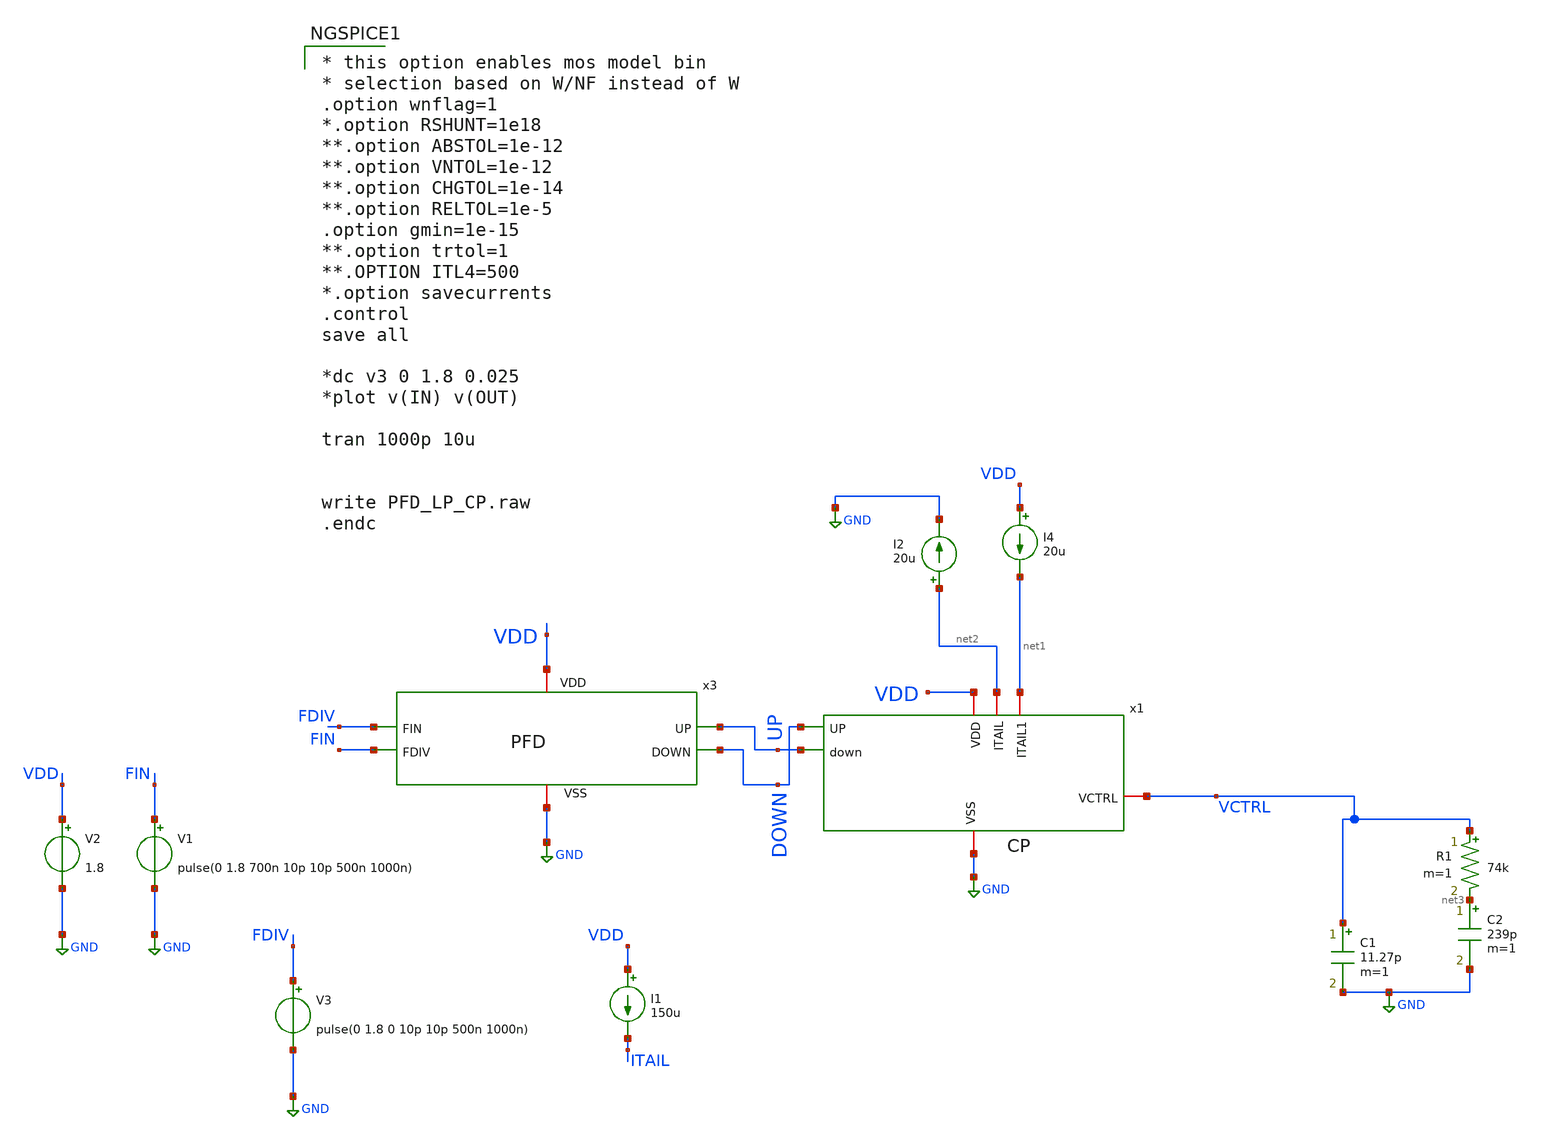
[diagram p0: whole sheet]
** sch_path: Xschem/CP_LP_PFD/PFD_LP_CP.sch
**.subckt PFD_LP_CP
x1 VDD net2 net1 VCTRL DOWN UP GND CP
x3 VDD GND FDIV FIN UP DOWN PFD
C1 VCTRL GND 11.27p m=1
R1 VCTRL net3 74k m=1
C2 net3 GND 239p m=1
V2 VDD GND 1.8
V1 FIN GND pulse(0 1.8 700n 10p 10p 500n 1000n)
V3 FDIV GND pulse(0 1.8 0 10p 10p 500n 1000n)
I1 VDD ITAIL 150u
I4 VDD net1 20u
I2 net2 GND 20u
**** begin user architecture code

** opencircuitdesign pdks install
.lib $::SKYWATER_MODELS/sky130.lib.spice tt



* this option enables mos model bin
* selection based on W/NF instead of W
.option wnflag=1
*.option RSHUNT=1e18
**.option ABSTOL=1e-12
**.option VNTOL=1e-12
**.option CHGTOL=1e-14
**.option RELTOL=1e-5
.option gmin=1e-15
**.option trtol=1
**.OPTION ITL4=500
*.option savecurrents
.control
save all

*dc v3 0 1.8 0.025
*plot v(IN) v(OUT)

tran 1000p 10u


write PFD_LP_CP.raw
.endc


**** end user architecture code
**.ends

* expanding   symbol:  CP.sym # of pins=7
** sym_path: CP.sym
** sch_path: CP.sch
.subckt CP VDD ITAIL ITAIL1 VCTRL UP down VSS
*.ipin UP
*.ipin down
*.iopin VCTRL
*.iopin VDD
*.iopin VSS
*.iopin ITAIL1
*.iopin ITAIL
XM8 net2 UP VDD VDD sky130_fd_pr__pfet_01v8 L=0.5 W=1 nf=1 ad='int((nf+1)/2) * W/nf * 0.29' as='int((nf+2)/2) * W/nf * 0.29'
+ pd='2*int((nf+1)/2) * (W/nf + 0.29)' ps='2*int((nf+2)/2) * (W/nf + 0.29)' nrd='0.29 / W' nrs='0.29 / W'
+ sa=0 sb=0 sd=0 mult=1 m=1
XM1 net1 net2 VDD VDD sky130_fd_pr__pfet_01v8 L=0.5 W=3 nf=1 ad='int((nf+1)/2) * W/nf * 0.29' as='int((nf+2)/2) * W/nf * 0.29'
+ pd='2*int((nf+1)/2) * (W/nf + 0.29)' ps='2*int((nf+2)/2) * (W/nf + 0.29)' nrd='0.29 / W' nrs='0.29 / W'
+ sa=0 sb=0 sd=0 mult=1 m=1
XM10 net2 UP VSS VSS sky130_fd_pr__nfet_01v8 L=0.5 W=0.5 nf=1 ad='int((nf+1)/2) * W/nf * 0.29' as='int((nf+2)/2) * W/nf * 0.29'
+ pd='2*int((nf+1)/2) * (W/nf + 0.29)' ps='2*int((nf+2)/2) * (W/nf + 0.29)' nrd='0.29 / W' nrs='0.29 / W'
+ sa=0 sb=0 sd=0 mult=1 m=1
XM2 VCTRL ITAIL net1 VDD sky130_fd_pr__pfet_01v8 L=0.5 W=2.5 nf=1 ad='int((nf+1)/2) * W/nf * 0.29' as='int((nf+2)/2) * W/nf * 0.29'
+ pd='2*int((nf+1)/2) * (W/nf + 0.29)' ps='2*int((nf+2)/2) * (W/nf + 0.29)' nrd='0.29 / W' nrs='0.29 / W'
+ sa=0 sb=0 sd=0 mult=1 m=1
XM3 ITAIL ITAIL VDD VDD sky130_fd_pr__pfet_01v8 L=0.5 W=2.5 nf=1 ad='int((nf+1)/2) * W/nf * 0.29' as='int((nf+2)/2) * W/nf * 0.29'
+ pd='2*int((nf+1)/2) * (W/nf + 0.29)' ps='2*int((nf+2)/2) * (W/nf + 0.29)' nrd='0.29 / W' nrs='0.29 / W'
+ sa=0 sb=0 sd=0 mult=1 m=1
XM5 ITAIL1 ITAIL1 VSS VSS sky130_fd_pr__nfet_01v8 L=0.5 W=1.5 nf=1 ad='int((nf+1)/2) * W/nf * 0.29' as='int((nf+2)/2) * W/nf * 0.29'
+ pd='2*int((nf+1)/2) * (W/nf + 0.29)' ps='2*int((nf+2)/2) * (W/nf + 0.29)' nrd='0.29 / W' nrs='0.29 / W'
+ sa=0 sb=0 sd=0 mult=1 m=1
XM6 VCTRL ITAIL1 net3 VSS sky130_fd_pr__nfet_01v8 L=0.5 W=1.5 nf=1 ad='int((nf+1)/2) * W/nf * 0.29' as='int((nf+2)/2) * W/nf * 0.29'
+ pd='2*int((nf+1)/2) * (W/nf + 0.29)' ps='2*int((nf+2)/2) * (W/nf + 0.29)' nrd='0.29 / W' nrs='0.29 / W'
+ sa=0 sb=0 sd=0 mult=1 m=1
XM4 net3 down VSS VSS sky130_fd_pr__nfet_01v8 L=0.5 W=1.5 nf=1 ad='int((nf+1)/2) * W/nf * 0.29' as='int((nf+2)/2) * W/nf * 0.29'
+ pd='2*int((nf+1)/2) * (W/nf + 0.29)' ps='2*int((nf+2)/2) * (W/nf + 0.29)' nrd='0.29 / W' nrs='0.29 / W'
+ sa=0 sb=0 sd=0 mult=1 m=1
.ends


* expanding   symbol:  PFD.sym # of pins=6
** sym_path: xschem/PFD.sym
** sch_path: xschem/PFD.sch
.subckt PFD VDD VSS FDIV FIN UP DOWN
*.ipin FDIV
*.ipin FIN
*.opin UP
*.opin DOWN
*.iopin VSS
*.iopin VDD
XM2 A FIN VDD VDD sky130_fd_pr__pfet_01v8 L=0.15 W=0.6 nf=1 ad='int((nf+1)/2) * W/nf * 0.29' as='int((nf+2)/2) * W/nf * 0.29'
+ pd='2*int((nf+1)/2) * (W/nf + 0.29)' ps='2*int((nf+2)/2) * (W/nf + 0.29)' nrd='0.29 / W' nrs='0.29 / W'
+ sa=0 sb=0 sd=0 mult=1 m=1
XM3 x1 A VDD VDD sky130_fd_pr__pfet_01v8 L=0.15 W=2.4 nf=1 ad='int((nf+1)/2) * W/nf * 0.29' as='int((nf+2)/2) * W/nf * 0.29'
+ pd='2*int((nf+1)/2) * (W/nf + 0.29)' ps='2*int((nf+2)/2) * (W/nf + 0.29)' nrd='0.29 / W' nrs='0.29 / W'
+ sa=0 sb=0 sd=0 mult=1 m=1
XM4 x1 x1 net1 VDD sky130_fd_pr__pfet_01v8 L=0.15 W=0.9 nf=1 ad='int((nf+1)/2) * W/nf * 0.29' as='int((nf+2)/2) * W/nf * 0.29'
+ pd='2*int((nf+1)/2) * (W/nf + 0.29)' ps='2*int((nf+2)/2) * (W/nf + 0.29)' nrd='0.29 / W' nrs='0.29 / W'
+ sa=0 sb=0 sd=0 mult=1 m=1
XM5 net1 x2 VDD VDD sky130_fd_pr__pfet_01v8 L=0.15 W=0.9 nf=1 ad='int((nf+1)/2) * W/nf * 0.29' as='int((nf+2)/2) * W/nf * 0.29'
+ pd='2*int((nf+1)/2) * (W/nf + 0.29)' ps='2*int((nf+2)/2) * (W/nf + 0.29)' nrd='0.29 / W' nrs='0.29 / W'
+ sa=0 sb=0 sd=0 mult=1 m=1
XM6 x3 x1 VDD VDD sky130_fd_pr__pfet_01v8 L=0.3 W=0.9 nf=1 ad='int((nf+1)/2) * W/nf * 0.29' as='int((nf+2)/2) * W/nf * 0.29'
+ pd='2*int((nf+1)/2) * (W/nf + 0.29)' ps='2*int((nf+2)/2) * (W/nf + 0.29)' nrd='0.29 / W' nrs='0.29 / W'
+ sa=0 sb=0 sd=0 mult=1 m=1
XM7 A x1b net2 VSS sky130_fd_pr__nfet_01v8 L=0.3 W=0.6 nf=1 ad='int((nf+1)/2) * W/nf * 0.29' as='int((nf+2)/2) * W/nf * 0.29'
+ pd='2*int((nf+1)/2) * (W/nf + 0.29)' ps='2*int((nf+2)/2) * (W/nf + 0.29)' nrd='0.29 / W' nrs='0.29 / W'
+ sa=0 sb=0 sd=0 mult=1 m=1
XM8 net2 x2b net12 VSS sky130_fd_pr__nfet_01v8 L=0.3 W=0.6 nf=1 ad='int((nf+1)/2) * W/nf * 0.29' as='int((nf+2)/2) * W/nf * 0.29'
+ pd='2*int((nf+1)/2) * (W/nf + 0.29)' ps='2*int((nf+2)/2) * (W/nf + 0.29)' nrd='0.29 / W' nrs='0.29 / W'
+ sa=0 sb=0 sd=0 mult=1 m=1
XM9 x1 FIN net3 VSS sky130_fd_pr__nfet_01v8 L=0.15 W=0.6 nf=1 ad='int((nf+1)/2) * W/nf * 0.29' as='int((nf+2)/2) * W/nf * 0.29'
+ pd='2*int((nf+1)/2) * (W/nf + 0.29)' ps='2*int((nf+2)/2) * (W/nf + 0.29)' nrd='0.29 / W' nrs='0.29 / W'
+ sa=0 sb=0 sd=0 mult=1 m=1
XM10 net3 A VSS VSS sky130_fd_pr__nfet_01v8 L=0.15 W=0.6 nf=1 ad='int((nf+1)/2) * W/nf * 0.29' as='int((nf+2)/2) * W/nf * 0.29'
+ pd='2*int((nf+1)/2) * (W/nf + 0.29)' ps='2*int((nf+2)/2) * (W/nf + 0.29)' nrd='0.29 / W' nrs='0.29 / W'
+ sa=0 sb=0 sd=0 mult=1 m=1
XM11 x3 x1 net4 VSS sky130_fd_pr__nfet_01v8 L=0.15 W=0.6 nf=1 ad='int((nf+1)/2) * W/nf * 0.29' as='int((nf+2)/2) * W/nf * 0.29'
+ pd='2*int((nf+1)/2) * (W/nf + 0.29)' ps='2*int((nf+2)/2) * (W/nf + 0.29)' nrd='0.29 / W' nrs='0.29 / W'
+ sa=0 sb=0 sd=0 mult=1 m=1
XM12 net4 x1 VSS VSS sky130_fd_pr__nfet_01v8 L=0.15 W=0.6 nf=1 ad='int((nf+1)/2) * W/nf * 0.29' as='int((nf+2)/2) * W/nf * 0.29'
+ pd='2*int((nf+1)/2) * (W/nf + 0.29)' ps='2*int((nf+2)/2) * (W/nf + 0.29)' nrd='0.29 / W' nrs='0.29 / W'
+ sa=0 sb=0 sd=0 mult=1 m=1
XM13 x3 x2b VSS VSS sky130_fd_pr__nfet_01v8 L=0.3 W=2.4 nf=1 ad='int((nf+1)/2) * W/nf * 0.29' as='int((nf+2)/2) * W/nf * 0.29'
+ pd='2*int((nf+1)/2) * (W/nf + 0.29)' ps='2*int((nf+2)/2) * (W/nf + 0.29)' nrd='0.29 / W' nrs='0.29 / W'
+ sa=0 sb=0 sd=0 mult=1 m=1
XM15 B FDIV VDD VDD sky130_fd_pr__pfet_01v8 L=0.15 W=0.6 nf=1 ad='int((nf+1)/2) * W/nf * 0.29' as='int((nf+2)/2) * W/nf * 0.29'
+ pd='2*int((nf+1)/2) * (W/nf + 0.29)' ps='2*int((nf+2)/2) * (W/nf + 0.29)' nrd='0.29 / W' nrs='0.29 / W'
+ sa=0 sb=0 sd=0 mult=1 m=1
XM16 x2 B VDD VDD sky130_fd_pr__pfet_01v8 L=0.15 W=2.4 nf=1 ad='int((nf+1)/2) * W/nf * 0.29' as='int((nf+2)/2) * W/nf * 0.29'
+ pd='2*int((nf+1)/2) * (W/nf + 0.29)' ps='2*int((nf+2)/2) * (W/nf + 0.29)' nrd='0.29 / W' nrs='0.29 / W'
+ sa=0 sb=0 sd=0 mult=1 m=1
XM17 x2 x2 net5 VDD sky130_fd_pr__pfet_01v8 L=0.15 W=0.9 nf=1 ad='int((nf+1)/2) * W/nf * 0.29' as='int((nf+2)/2) * W/nf * 0.29'
+ pd='2*int((nf+1)/2) * (W/nf + 0.29)' ps='2*int((nf+2)/2) * (W/nf + 0.29)' nrd='0.29 / W' nrs='0.29 / W'
+ sa=0 sb=0 sd=0 mult=1 m=1
XM18 net5 x1 VDD VDD sky130_fd_pr__pfet_01v8 L=0.15 W=0.9 nf=1 ad='int((nf+1)/2) * W/nf * 0.29' as='int((nf+2)/2) * W/nf * 0.29'
+ pd='2*int((nf+1)/2) * (W/nf + 0.29)' ps='2*int((nf+2)/2) * (W/nf + 0.29)' nrd='0.29 / W' nrs='0.29 / W'
+ sa=0 sb=0 sd=0 mult=1 m=1
XM19 x4 x2 VDD VDD sky130_fd_pr__pfet_01v8 L=0.3 W=0.9 nf=1 ad='int((nf+1)/2) * W/nf * 0.29' as='int((nf+2)/2) * W/nf * 0.29'
+ pd='2*int((nf+1)/2) * (W/nf + 0.29)' ps='2*int((nf+2)/2) * (W/nf + 0.29)' nrd='0.29 / W' nrs='0.29 / W'
+ sa=0 sb=0 sd=0 mult=1 m=1
XM20 B x2b net6 VSS sky130_fd_pr__nfet_01v8 L=0.3 W=0.6 nf=1 ad='int((nf+1)/2) * W/nf * 0.29' as='int((nf+2)/2) * W/nf * 0.29'
+ pd='2*int((nf+1)/2) * (W/nf + 0.29)' ps='2*int((nf+2)/2) * (W/nf + 0.29)' nrd='0.29 / W' nrs='0.29 / W'
+ sa=0 sb=0 sd=0 mult=1 m=1
XM21 net6 x1b net11 VSS sky130_fd_pr__nfet_01v8 L=0.3 W=0.6 nf=1 ad='int((nf+1)/2) * W/nf * 0.29' as='int((nf+2)/2) * W/nf * 0.29'
+ pd='2*int((nf+1)/2) * (W/nf + 0.29)' ps='2*int((nf+2)/2) * (W/nf + 0.29)' nrd='0.29 / W' nrs='0.29 / W'
+ sa=0 sb=0 sd=0 mult=1 m=1
XM22 x2 FDIV net8 VSS sky130_fd_pr__nfet_01v8 L=0.15 W=0.6 nf=1 ad='int((nf+1)/2) * W/nf * 0.29' as='int((nf+2)/2) * W/nf * 0.29'
+ pd='2*int((nf+1)/2) * (W/nf + 0.29)' ps='2*int((nf+2)/2) * (W/nf + 0.29)' nrd='0.29 / W' nrs='0.29 / W'
+ sa=0 sb=0 sd=0 mult=1 m=1
XM23 net8 B VSS VSS sky130_fd_pr__nfet_01v8 L=0.15 W=0.6 nf=1 ad='int((nf+1)/2) * W/nf * 0.29' as='int((nf+2)/2) * W/nf * 0.29'
+ pd='2*int((nf+1)/2) * (W/nf + 0.29)' ps='2*int((nf+2)/2) * (W/nf + 0.29)' nrd='0.29 / W' nrs='0.29 / W'
+ sa=0 sb=0 sd=0 mult=1 m=1
XM24 x4 x2 net7 VSS sky130_fd_pr__nfet_01v8 L=0.15 W=0.6 nf=1 ad='int((nf+1)/2) * W/nf * 0.29' as='int((nf+2)/2) * W/nf * 0.29'
+ pd='2*int((nf+1)/2) * (W/nf + 0.29)' ps='2*int((nf+2)/2) * (W/nf + 0.29)' nrd='0.29 / W' nrs='0.29 / W'
+ sa=0 sb=0 sd=0 mult=1 m=1
XM25 net7 x2 VSS VSS sky130_fd_pr__nfet_01v8 L=0.15 W=0.6 nf=1 ad='int((nf+1)/2) * W/nf * 0.29' as='int((nf+2)/2) * W/nf * 0.29'
+ pd='2*int((nf+1)/2) * (W/nf + 0.29)' ps='2*int((nf+2)/2) * (W/nf + 0.29)' nrd='0.29 / W' nrs='0.29 / W'
+ sa=0 sb=0 sd=0 mult=1 m=1
XM26 x4 x1b VSS VSS sky130_fd_pr__nfet_01v8 L=0.3 W=2.4 nf=1 ad='int((nf+1)/2) * W/nf * 0.29' as='int((nf+2)/2) * W/nf * 0.29'
+ pd='2*int((nf+1)/2) * (W/nf + 0.29)' ps='2*int((nf+2)/2) * (W/nf + 0.29)' nrd='0.29 / W' nrs='0.29 / W'
+ sa=0 sb=0 sd=0 mult=1 m=1
XM1 net11 FDIV VSS VSS sky130_fd_pr__nfet_01v8 L=0.3 W=0.6 nf=1 ad='int((nf+1)/2) * W/nf * 0.29' as='int((nf+2)/2) * W/nf * 0.29'
+ pd='2*int((nf+1)/2) * (W/nf + 0.29)' ps='2*int((nf+2)/2) * (W/nf + 0.29)' nrd='0.29 / W' nrs='0.29 / W'
+ sa=0 sb=0 sd=0 mult=1 m=1
XM14 net12 FIN VSS VSS sky130_fd_pr__nfet_01v8 L=0.3 W=0.6 nf=1 ad='int((nf+1)/2) * W/nf * 0.29' as='int((nf+2)/2) * W/nf * 0.29'
+ pd='2*int((nf+1)/2) * (W/nf + 0.29)' ps='2*int((nf+2)/2) * (W/nf + 0.29)' nrd='0.29 / W' nrs='0.29 / W'
+ sa=0 sb=0 sd=0 mult=1 m=1
x1 VDD VSS x1 x1b PFD_INV
x2 VDD VSS x2 x2b PFD_INV
x3 VDD VSS x3 net10 PFD_INV
x5 VDD VSS x4 net9 PFD_INV
x6 VDD VSS net9 DOWN PFD_INV
x4 VDD VSS net10 UP PFD_INV
.ends


* expanding   symbol:  PFD_INV.sym # of pins=4
** sym_path: PFD_INV.sym
** sch_path: PFD_INV.sch
.subckt PFD_INV VDD VSS IN OUT
*.iopin VDD
*.iopin VSS
*.ipin IN
*.opin OUT
XM1 OUT IN VDD VDD sky130_fd_pr__pfet_01v8 L=0.15 W=0.8 nf=1 ad='int((nf+1)/2) * W/nf * 0.29' as='int((nf+2)/2) * W/nf * 0.29'
+ pd='2*int((nf+1)/2) * (W/nf + 0.29)' ps='2*int((nf+2)/2) * (W/nf + 0.29)' nrd='0.29 / W' nrs='0.29 / W'
+ sa=0 sb=0 sd=0 mult=1 m=1
XM3 OUT IN VSS VSS sky130_fd_pr__nfet_01v8 L=0.15 W=0.4 nf=1 ad='int((nf+1)/2) * W/nf * 0.29' as='int((nf+2)/2) * W/nf * 0.29'
+ pd='2*int((nf+1)/2) * (W/nf + 0.29)' ps='2*int((nf+2)/2) * (W/nf + 0.29)' nrd='0.29 / W' nrs='0.29 / W'
+ sa=0 sb=0 sd=0 mult=1 m=1
.ends

.GLOBAL GND
.end
